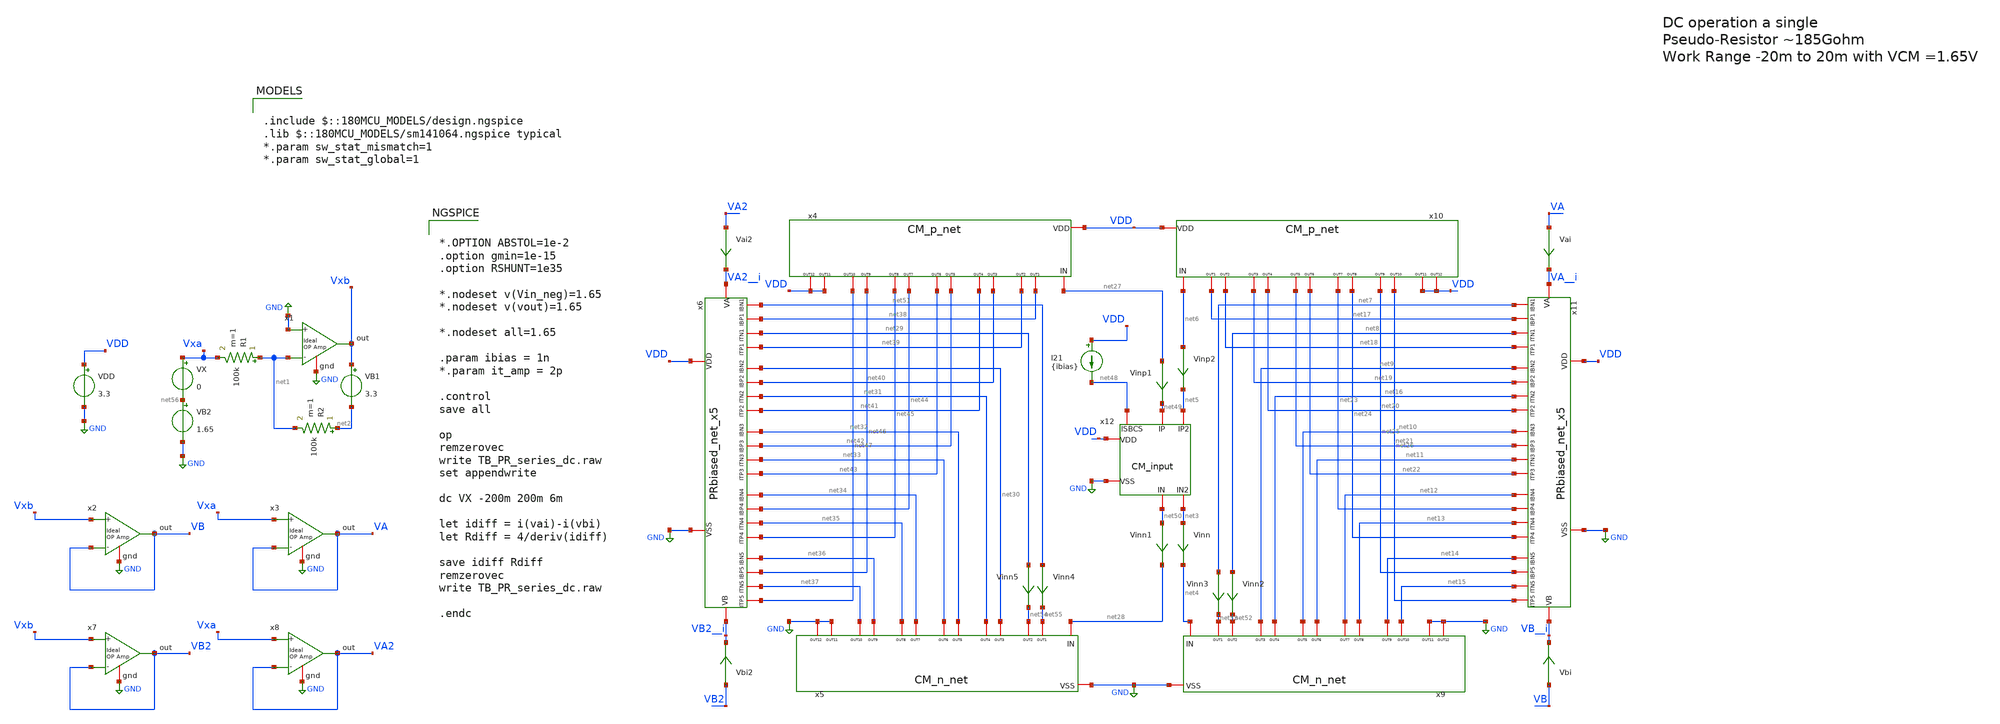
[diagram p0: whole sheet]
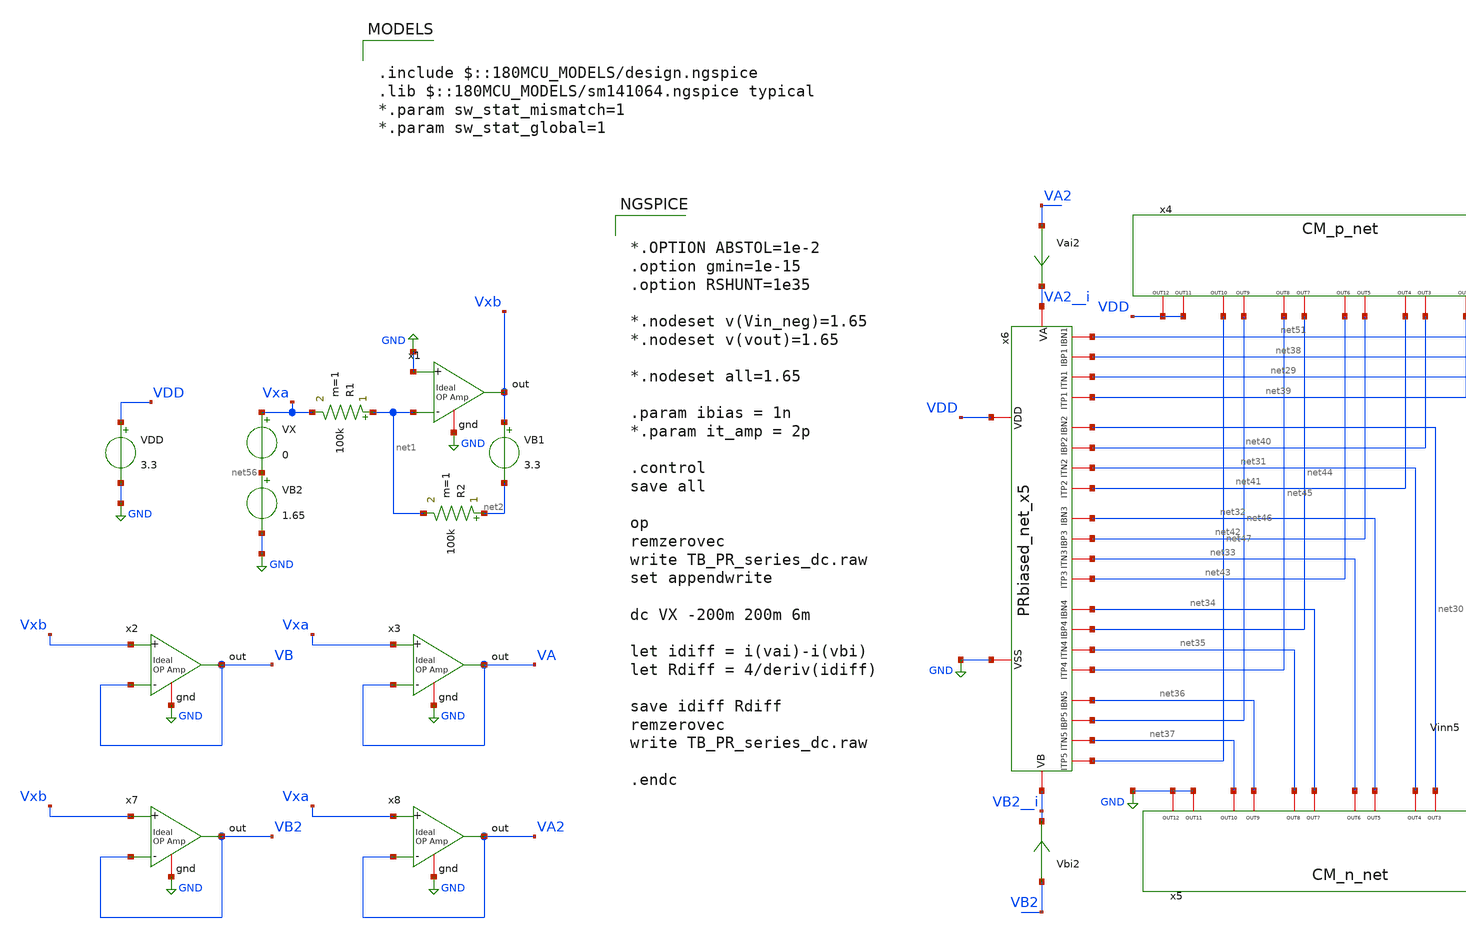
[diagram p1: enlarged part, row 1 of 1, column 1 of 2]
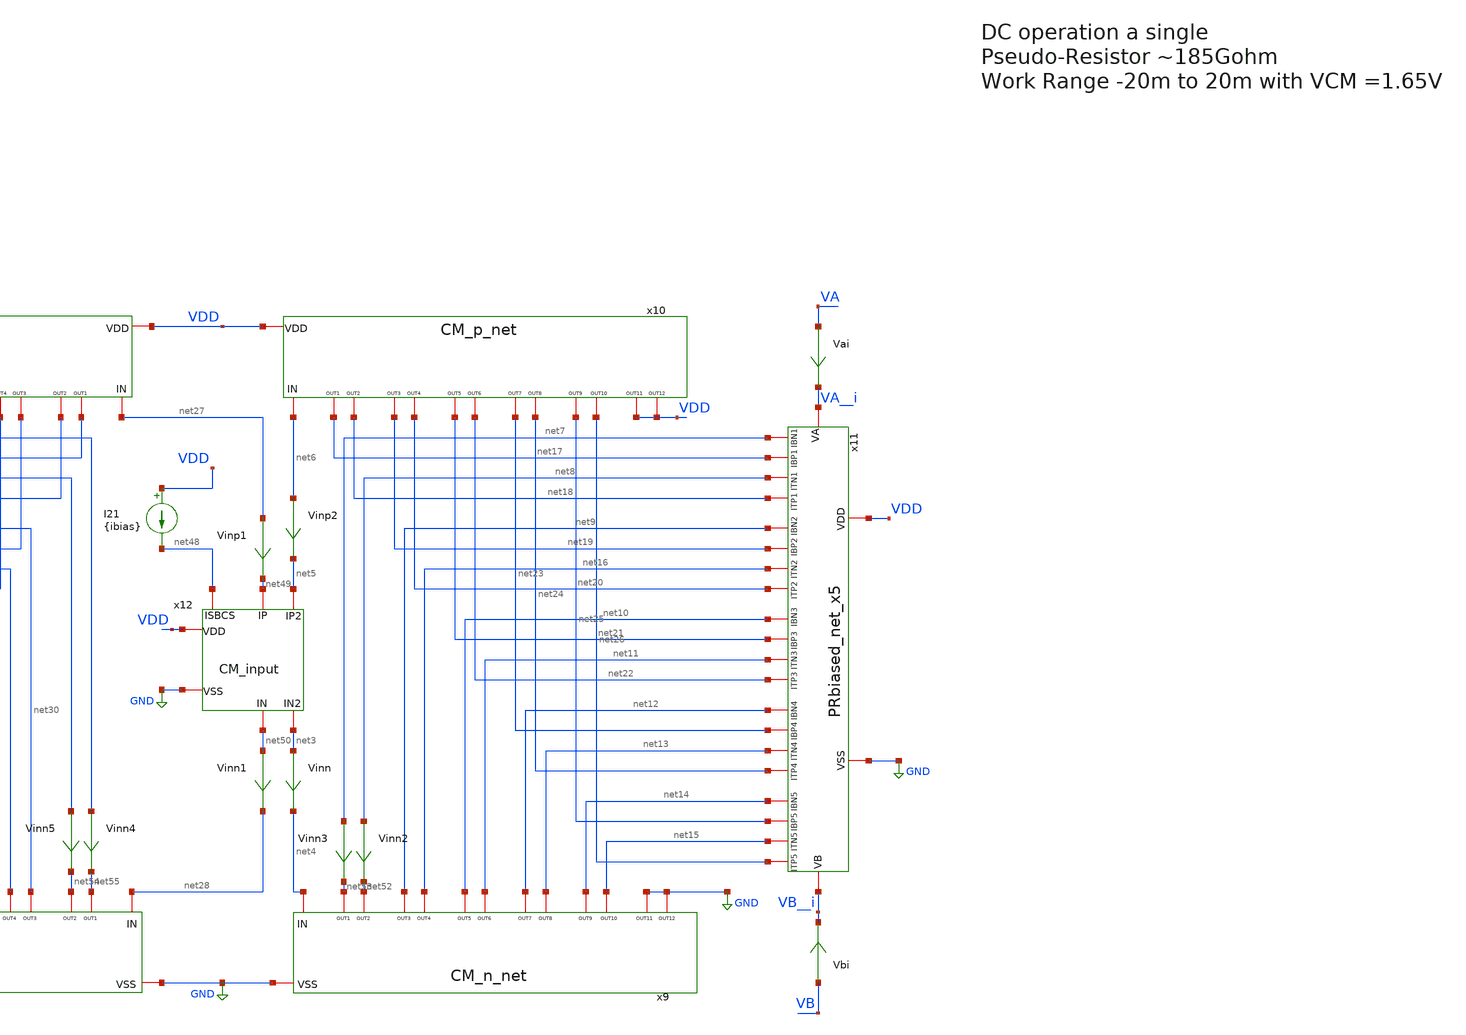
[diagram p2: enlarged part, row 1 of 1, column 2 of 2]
** sch_path: TIA_Filter/PseudoResistor/TB_PR_series_dc.sch
**.subckt TB_PR_series_dc
VDD VDD GND 3.3
VX Vxa net56 0
VB1 Vxb net2 3.3
R1 net1 Vxa 100k m=1
R2 net2 net1 100k m=1
VB2 net56 GND 1.65
x2 VB Vxb VB GND ampOp_ideal
x3 VA Vxa VA GND ampOp_ideal
x1 Vxb GND net1 GND ampOp_ideal
x9 net4 net53 net52 net9 net16 net10 net11 net12 net13 net14 net15 GND GND GND CM_n_net
x10 net6 net17 net18 net19 net20 net21 net22 net23 net24 net25 net26 VDD VDD VDD CM_p_net
x11 VA__i VB__i net10 net9 net7 net14 net12 net21 net19 net23 net17 net25 net11 net8 net15 net16
+ net13 net26 net20 net18 net24 net22 VDD GND PRbiased_net_x5
x12 net49 net5 net50 net3 net48 VDD GND CM_input
x4 net27 net38 net39 net40 net41 net42 net43 net44 net45 net46 net47 VDD VDD VDD CM_p_net
x5 net28 net55 net54 net30 net31 net32 net33 net34 net35 net36 net37 GND GND GND CM_n_net
x6 VA2__i VB2__i net32 net30 net51 net36 net34 net42 net40 net44 net38 net46 net33 net29 net37 net31
+ net35 net47 net41 net39 net45 net43 VDD GND PRbiased_net_x5
I21 VDD net48 {ibias}
Vinn net3 net4 0
.save i(vinn)
Vinp1 net27 net49 0
.save i(vinp1)
Vinp2 net6 net5 0
.save i(vinp2)
Vinn1 net50 net28 0
.save i(vinn1)
Vai VA VA__i 0
.save i(vai)
Vbi VB VB__i 0
.save i(vbi)
Vbi2 VB2 VB2__i 0
.save i(vbi2)
Vai2 VA2 VA2__i 0
.save i(vai2)
x7 VB2 Vxb VB2 GND ampOp_ideal
x8 VA2 Vxa VA2 GND ampOp_ideal
Vinn2 net8 net52 0
.save i(vinn2)
Vinn3 net7 net53 0
.save i(vinn3)
Vinn4 net51 net55 0
.save i(vinn4)
Vinn5 net29 net54 0
.save i(vinn5)
**** begin user architecture code

.include $::180MCU_MODELS/design.ngspice
.lib $::180MCU_MODELS/sm141064.ngspice typical
*.param sw_stat_mismatch=1
*.param sw_stat_global=1



*.OPTION ABSTOL=1e-2
.option gmin=1e-15
.option RSHUNT=1e35

*.nodeset v(Vin_neg)=1.65
*.nodeset v(vout)=1.65

*.nodeset all=1.65

.param ibias = 1n
*.param it_amp = 2p

.control
save all

op
remzerovec
write TB_PR_series_dc.raw
set appendwrite

dc VX -200m 200m 6m

let idiff = i(vai)-i(vbi)
let Rdiff = 4/deriv(idiff)

save idiff Rdiff
remzerovec
write TB_PR_series_dc.raw

.endc


**** end user architecture code
**.ends
.GLOBAL GND
.end
